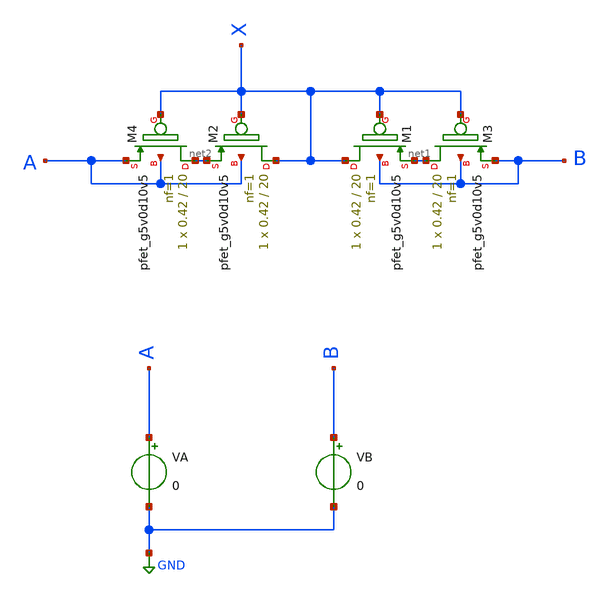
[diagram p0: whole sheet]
** sch_path: xschem/MISC/pseudo/pseudo_tb.sch
* Copyright 2020 Stefan Frederik Schippers
* Licensed under the Apache License, Version 2.0 (the "License");
* you may not use this file except in compliance with the License.
* You may obtain a copy of the License at
* https://www.apache.org/licenses/LICENSE-2.0
* Unless required by applicable law or agreed to in writing, software
* distributed under the License is distributed on an "AS IS" BASIS,
* WITHOUT WARRANTIES OR CONDITIONS OF ANY KIND, either express or implied.
* See the License for the specific language governing permissions and
* limitations under the License.
**.subckt pseudo_tb
XM1 X X net1 B sky130_fd_pr__pfet_g5v0d10v5 L=20 W=0.42 nf=1 ad='int((nf+1)/2) * W/nf * 0.29' as='int((nf+2)/2) * W/nf * 0.29'
+ pd='2*int((nf+1)/2) * (W/nf + 0.29)' ps='2*int((nf+2)/2) * (W/nf + 0.29)' nrd='0.29 / W' nrs='0.29 / W'
+ sa=0 sb=0 sd=0 mult=1 m=1
XM2 X X net2 A sky130_fd_pr__pfet_g5v0d10v5 L=20 W=0.42 nf=1 ad='int((nf+1)/2) * W/nf * 0.29' as='int((nf+2)/2) * W/nf * 0.29'
+ pd='2*int((nf+1)/2) * (W/nf + 0.29)' ps='2*int((nf+2)/2) * (W/nf + 0.29)' nrd='0.29 / W' nrs='0.29 / W'
+ sa=0 sb=0 sd=0 mult=1 m=1
VA A GND 0
VB B GND 0
XM3 net1 X B B sky130_fd_pr__pfet_g5v0d10v5 L=20 W=0.42 nf=1 ad='int((nf+1)/2) * W/nf * 0.29' as='int((nf+2)/2) * W/nf * 0.29'
+ pd='2*int((nf+1)/2) * (W/nf + 0.29)' ps='2*int((nf+2)/2) * (W/nf + 0.29)' nrd='0.29 / W' nrs='0.29 / W'
+ sa=0 sb=0 sd=0 mult=1 m=1
XM4 net2 X A A sky130_fd_pr__pfet_g5v0d10v5 L=20 W=0.42 nf=1 ad='int((nf+1)/2) * W/nf * 0.29' as='int((nf+2)/2) * W/nf * 0.29'
+ pd='2*int((nf+1)/2) * (W/nf + 0.29)' ps='2*int((nf+2)/2) * (W/nf + 0.29)' nrd='0.29 / W' nrs='0.29 / W'
+ sa=0 sb=0 sd=0 mult=1 m=1
**** begin user architecture code



.include /usr/share/pdk/sky130A/libs.ref/spi/sky130_fd_pr/sky130_fd_pr__pfet_g5v0d10v5__tt.corner.spice
.include /usr/share/pdk/sky130A/libs.ref/spi/sky130_fd_pr/sky130_fd_pr__pfet_g5v0d10v5__mismatch.corner.spice
.include /usr/share/pdk/sky130A/libs.ref/spi/sky130_fd_pr/sky130_fd_pr__nfet_g5v0d10v5__tt.corner.spice
.include /usr/share/pdk/sky130A/libs.ref/spi/sky130_fd_pr/sky130_fd_pr__nfet_g5v0d10v5__mismatch.corner.spice

.include /usr/share/pdk/sky130A/libs.ref/spi/sky130_fd_pr/sky130_fd_pr__nfet_01v8_lvt__tt.corner.spice
.include /usr/share/pdk/sky130A/libs.ref/spi/sky130_fd_pr/sky130_fd_pr__nfet_01v8_lvt__mismatch.corner.spice
.include /usr/share/pdk/sky130A/libs.ref/spi/sky130_fd_pr/sky130_fd_pr__pfet_01v8_lvt__tt.corner.spice
.include /usr/share/pdk/sky130A/libs.ref/spi/sky130_fd_pr/sky130_fd_pr__pfet_01v8_lvt__mismatch.corner.spice

.include ~/OpenPDK/skywater-pdk/skywater-pdk/libraries/sky130_fd_pr/latest/models/all.spice





.options gmin=1e-14
.options rshunt = 1.0e14

.control
  dc VA -0.1 0.1 0.011
  let r=abs(deriv(v(a))/deriv(i(va)))
  plot r ylog
.endc


**** end user architecture code
**.ends
.GLOBAL GND
.end
